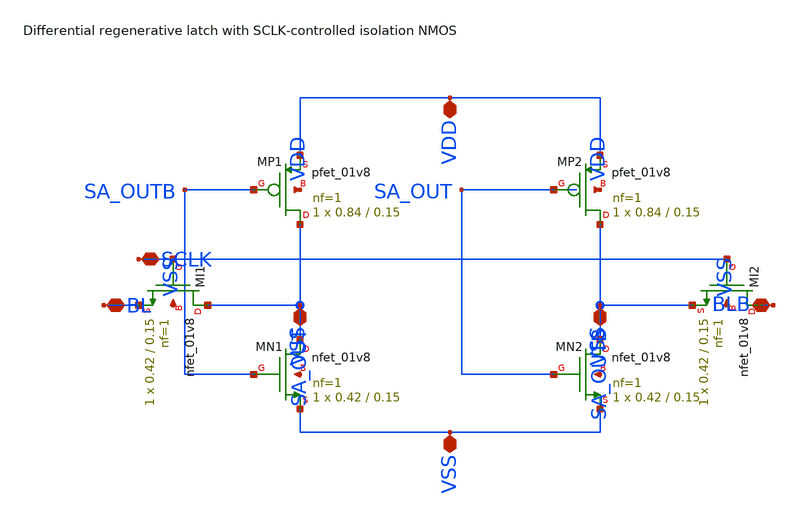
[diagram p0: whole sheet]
** sch_path: cells/experimental/sense_amp_nmos_isolation.sch
**.subckt sense_amp_nmos_isolation VDD VSS BL BLB SCLK SA_OUT SA_OUTB
*.iopin VDD
*.iopin VSS
*.iopin BL
*.iopin BLB
*.iopin SCLK
*.iopin SA_OUT
*.iopin SA_OUTB
XMP1 SA_OUT SA_OUTB VDD VDD sky130_fd_pr__pfet_01v8 L=0.15 W=0.84 nf=1 ad='int((nf+1)/2) * W/nf * 0.29'
+ as='int((nf+2)/2) * W/nf * 0.29' pd='2*int((nf+1)/2) * (W/nf + 0.29)' ps='2*int((nf+2)/2) * (W/nf + 0.29)'
+ nrd='0.29 / W' nrs='0.29 / W' sa=0 sb=0 sd=0 mult=1 m=1
XMN1 SA_OUT SA_OUTB VSS VSS sky130_fd_pr__nfet_01v8 L=0.15 W=0.42 nf=1 ad='int((1 + 1)/2) * 0.42 / 1 * 0.29'
+ as='int((1 + 2)/2) * 0.42 / 1 * 0.29' pd='2*int((1 + 1)/2) * (0.42 / 1 + 0.29)' ps='2*int((1 + 2)/2) * (0.42 / 1 + 0.29)'
+ nrd='0.29 / 0.42 ' nrs='0.29 / 0.42 ' sa=0 sb=0 sd=0 mult=1 m=1
XMP2 SA_OUTB SA_OUT VDD VDD sky130_fd_pr__pfet_01v8 L=0.15 W=0.84 nf=1 ad='int((nf+1)/2) * W/nf * 0.29'
+ as='int((nf+2)/2) * W/nf * 0.29' pd='2*int((nf+1)/2) * (W/nf + 0.29)' ps='2*int((nf+2)/2) * (W/nf + 0.29)'
+ nrd='0.29 / W' nrs='0.29 / W' sa=0 sb=0 sd=0 mult=1 m=1
XMN2 SA_OUTB SA_OUT VSS VSS sky130_fd_pr__nfet_01v8 L=0.15 W=0.42 nf=1 ad='int((1 + 1)/2) * 0.42 / 1 * 0.29'
+ as='int((1 + 2)/2) * 0.42 / 1 * 0.29' pd='2*int((1 + 1)/2) * (0.42 / 1 + 0.29)' ps='2*int((1 + 2)/2) * (0.42 / 1 + 0.29)'
+ nrd='0.29 / 0.42 ' nrs='0.29 / 0.42 ' sa=0 sb=0 sd=0 mult=1 m=1
XMI1 SA_OUT SCLK BL VSS sky130_fd_pr__nfet_01v8 L=0.15 W=0.42 nf=1 ad='int((1 + 1)/2) * 0.42 / 1 * 0.29'
+ as='int((1 + 2)/2) * 0.42 / 1 * 0.29' pd='2*int((1 + 1)/2) * (0.42 / 1 + 0.29)' ps='2*int((1 + 2)/2) * (0.42 / 1 + 0.29)'
+ nrd='0.29 / 0.42 ' nrs='0.29 / 0.42 ' sa=0 sb=0 sd=0 mult=1 m=1
XMI2 BLB SCLK SA_OUTB VSS sky130_fd_pr__nfet_01v8 L=0.15 W=0.42 nf=1 ad='int((1 + 1)/2) * 0.42 / 1 * 0.29'
+ as='int((1 + 2)/2) * 0.42 / 1 * 0.29' pd='2*int((1 + 1)/2) * (0.42 / 1 + 0.29)' ps='2*int((1 + 2)/2) * (0.42 / 1 + 0.29)'
+ nrd='0.29 / 0.42 ' nrs='0.29 / 0.42 ' sa=0 sb=0 sd=0 mult=1 m=1
**.ends
.end
